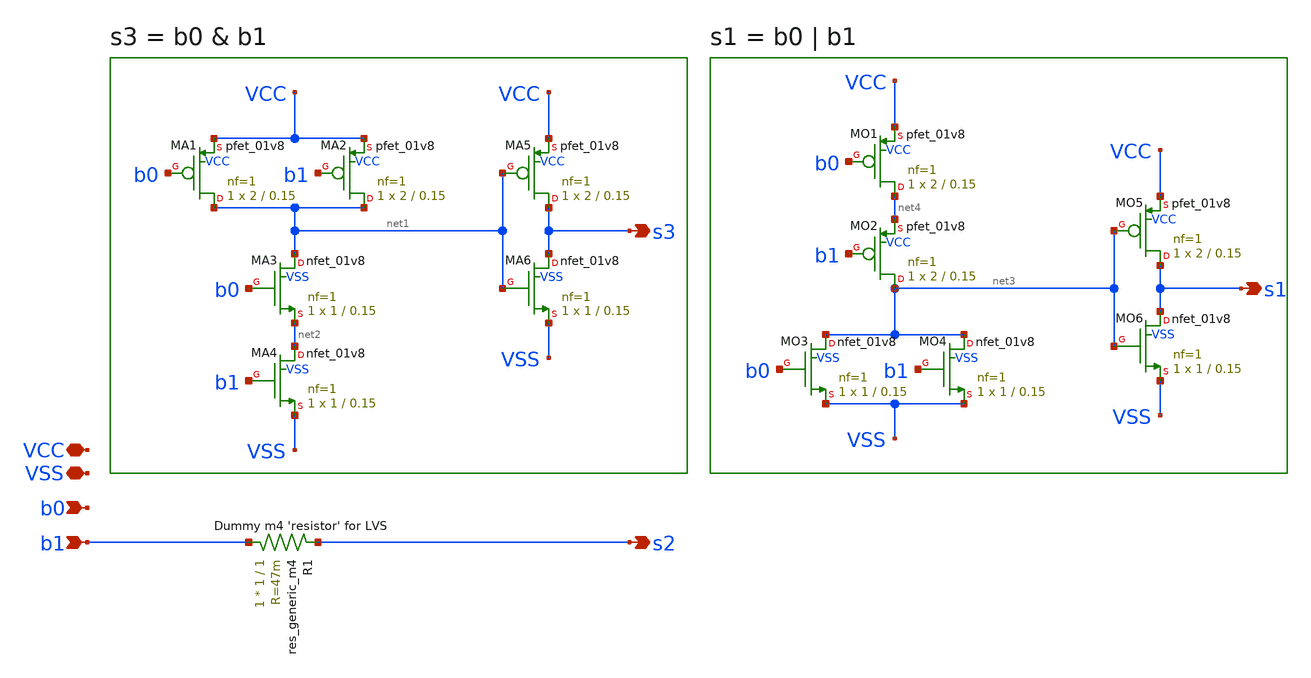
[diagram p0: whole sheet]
** sch_path: xschem/thermo2bit.sch
**.subckt thermo2bit b1 s2 b0 s3 VCC VSS s1
*.ipin b1
*.opin s2
*.ipin b0
*.opin s3
*.iopin VCC
*.iopin VSS
*.opin s1
XMA1 net1 b0 VCC VCC sky130_fd_pr__pfet_01v8 L=0.15 W=2 nf=1 ad='int((nf+1)/2) * W/nf * 0.29' as='int((nf+2)/2) * W/nf * 0.29'
+ pd='2*int((nf+1)/2) * (W/nf + 0.29)' ps='2*int((nf+2)/2) * (W/nf + 0.29)' nrd='0.29 / W' nrs='0.29 / W'
+ sa=0 sb=0 sd=0 mult=1 m=1
XMA3 net1 b0 net2 VSS sky130_fd_pr__nfet_01v8 L=0.15 W=1 nf=1 ad='int((nf+1)/2) * W/nf * 0.29' as='int((nf+2)/2) * W/nf * 0.29'
+ pd='2*int((nf+1)/2) * (W/nf + 0.29)' ps='2*int((nf+2)/2) * (W/nf + 0.29)' nrd='0.29 / W' nrs='0.29 / W'
+ sa=0 sb=0 sd=0 mult=1 m=1
XMA2 net1 b1 VCC VCC sky130_fd_pr__pfet_01v8 L=0.15 W=2 nf=1 ad='int((nf+1)/2) * W/nf * 0.29' as='int((nf+2)/2) * W/nf * 0.29'
+ pd='2*int((nf+1)/2) * (W/nf + 0.29)' ps='2*int((nf+2)/2) * (W/nf + 0.29)' nrd='0.29 / W' nrs='0.29 / W'
+ sa=0 sb=0 sd=0 mult=1 m=1
XMA4 net2 b1 VSS VSS sky130_fd_pr__nfet_01v8 L=0.15 W=1 nf=1 ad='int((nf+1)/2) * W/nf * 0.29' as='int((nf+2)/2) * W/nf * 0.29'
+ pd='2*int((nf+1)/2) * (W/nf + 0.29)' ps='2*int((nf+2)/2) * (W/nf + 0.29)' nrd='0.29 / W' nrs='0.29 / W'
+ sa=0 sb=0 sd=0 mult=1 m=1
XMA5 s3 net1 VCC VCC sky130_fd_pr__pfet_01v8 L=0.15 W=2 nf=1 ad='int((nf+1)/2) * W/nf * 0.29' as='int((nf+2)/2) * W/nf * 0.29'
+ pd='2*int((nf+1)/2) * (W/nf + 0.29)' ps='2*int((nf+2)/2) * (W/nf + 0.29)' nrd='0.29 / W' nrs='0.29 / W'
+ sa=0 sb=0 sd=0 mult=1 m=1
XMA6 s3 net1 VSS VSS sky130_fd_pr__nfet_01v8 L=0.15 W=1 nf=1 ad='int((nf+1)/2) * W/nf * 0.29' as='int((nf+2)/2) * W/nf * 0.29'
+ pd='2*int((nf+1)/2) * (W/nf + 0.29)' ps='2*int((nf+2)/2) * (W/nf + 0.29)' nrd='0.29 / W' nrs='0.29 / W'
+ sa=0 sb=0 sd=0 mult=1 m=1
XMO5 s1 net3 VCC VCC sky130_fd_pr__pfet_01v8 L=0.15 W=2 nf=1 ad='int((nf+1)/2) * W/nf * 0.29' as='int((nf+2)/2) * W/nf * 0.29'
+ pd='2*int((nf+1)/2) * (W/nf + 0.29)' ps='2*int((nf+2)/2) * (W/nf + 0.29)' nrd='0.29 / W' nrs='0.29 / W'
+ sa=0 sb=0 sd=0 mult=1 m=1
XMO6 s1 net3 VSS VSS sky130_fd_pr__nfet_01v8 L=0.15 W=1 nf=1 ad='int((nf+1)/2) * W/nf * 0.29' as='int((nf+2)/2) * W/nf * 0.29'
+ pd='2*int((nf+1)/2) * (W/nf + 0.29)' ps='2*int((nf+2)/2) * (W/nf + 0.29)' nrd='0.29 / W' nrs='0.29 / W'
+ sa=0 sb=0 sd=0 mult=1 m=1
XMO1 net4 b0 VCC VCC sky130_fd_pr__pfet_01v8 L=0.15 W=2 nf=1 ad='int((nf+1)/2) * W/nf * 0.29' as='int((nf+2)/2) * W/nf * 0.29'
+ pd='2*int((nf+1)/2) * (W/nf + 0.29)' ps='2*int((nf+2)/2) * (W/nf + 0.29)' nrd='0.29 / W' nrs='0.29 / W'
+ sa=0 sb=0 sd=0 mult=1 m=1
XMO2 net3 b1 net4 VCC sky130_fd_pr__pfet_01v8 L=0.15 W=2 nf=1 ad='int((nf+1)/2) * W/nf * 0.29' as='int((nf+2)/2) * W/nf * 0.29'
+ pd='2*int((nf+1)/2) * (W/nf + 0.29)' ps='2*int((nf+2)/2) * (W/nf + 0.29)' nrd='0.29 / W' nrs='0.29 / W'
+ sa=0 sb=0 sd=0 mult=1 m=1
XMO3 net3 b0 VSS VSS sky130_fd_pr__nfet_01v8 L=0.15 W=1 nf=1 ad='int((nf+1)/2) * W/nf * 0.29' as='int((nf+2)/2) * W/nf * 0.29'
+ pd='2*int((nf+1)/2) * (W/nf + 0.29)' ps='2*int((nf+2)/2) * (W/nf + 0.29)' nrd='0.29 / W' nrs='0.29 / W'
+ sa=0 sb=0 sd=0 mult=1 m=1
XMO4 net3 b1 VSS VSS sky130_fd_pr__nfet_01v8 L=0.15 W=1 nf=1 ad='int((nf+1)/2) * W/nf * 0.29' as='int((nf+2)/2) * W/nf * 0.29'
+ pd='2*int((nf+1)/2) * (W/nf + 0.29)' ps='2*int((nf+2)/2) * (W/nf + 0.29)' nrd='0.29 / W' nrs='0.29 / W'
+ sa=0 sb=0 sd=0 mult=1 m=1
R1 b1 s2 sky130_fd_pr__res_generic_m4 W=1 L=1 m=1
**.ends
.end
